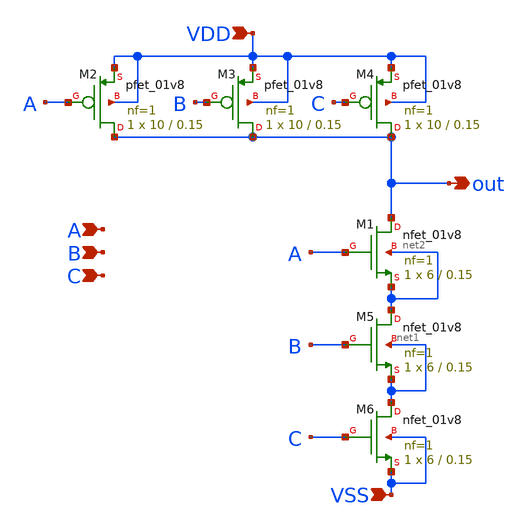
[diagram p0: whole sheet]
** sch_path: nand/nand3.sch
**.subckt nand3 A B C VSS VDD out
*.ipin A
*.ipin B
*.ipin C
*.ipin VSS
*.ipin VDD
*.opin out
XM1 out A net2 net2 sky130_fd_pr__nfet_01v8 L=0.15 W=6 nf=1 ad='int((nf+1)/2) * W/nf * 0.29' as='int((nf+2)/2) * W/nf * 0.29'
+ pd='2*int((nf+1)/2) * (W/nf + 0.29)' ps='2*int((nf+2)/2) * (W/nf + 0.29)' nrd='0.29 / W' nrs='0.29 / W'
+ sa=0 sb=0 sd=0 mult=1 m=1
XM2 out A VDD VDD sky130_fd_pr__pfet_01v8 L=0.15 W=10 nf=1 ad='int((nf+1)/2) * W/nf * 0.29' as='int((nf+2)/2) * W/nf * 0.29'
+ pd='2*int((nf+1)/2) * (W/nf + 0.29)' ps='2*int((nf+2)/2) * (W/nf + 0.29)' nrd='0.29 / W' nrs='0.29 / W'
+ sa=0 sb=0 sd=0 mult=1 m=1
XM3 out B VDD VDD sky130_fd_pr__pfet_01v8 L=0.15 W=10 nf=1 ad='int((nf+1)/2) * W/nf * 0.29' as='int((nf+2)/2) * W/nf * 0.29'
+ pd='2*int((nf+1)/2) * (W/nf + 0.29)' ps='2*int((nf+2)/2) * (W/nf + 0.29)' nrd='0.29 / W' nrs='0.29 / W'
+ sa=0 sb=0 sd=0 mult=1 m=1
XM4 out C VDD VDD sky130_fd_pr__pfet_01v8 L=0.15 W=10 nf=1 ad='int((nf+1)/2) * W/nf * 0.29' as='int((nf+2)/2) * W/nf * 0.29'
+ pd='2*int((nf+1)/2) * (W/nf + 0.29)' ps='2*int((nf+2)/2) * (W/nf + 0.29)' nrd='0.29 / W' nrs='0.29 / W'
+ sa=0 sb=0 sd=0 mult=1 m=1
XM5 net2 B net1 net1 sky130_fd_pr__nfet_01v8 L=0.15 W=6 nf=1 ad='int((nf+1)/2) * W/nf * 0.29' as='int((nf+2)/2) * W/nf * 0.29'
+ pd='2*int((nf+1)/2) * (W/nf + 0.29)' ps='2*int((nf+2)/2) * (W/nf + 0.29)' nrd='0.29 / W' nrs='0.29 / W'
+ sa=0 sb=0 sd=0 mult=1 m=1
XM6 net1 C VSS VSS sky130_fd_pr__nfet_01v8 L=0.15 W=6 nf=1 ad='int((nf+1)/2) * W/nf * 0.29' as='int((nf+2)/2) * W/nf * 0.29'
+ pd='2*int((nf+1)/2) * (W/nf + 0.29)' ps='2*int((nf+2)/2) * (W/nf + 0.29)' nrd='0.29 / W' nrs='0.29 / W'
+ sa=0 sb=0 sd=0 mult=1 m=1
**.ends
.end
